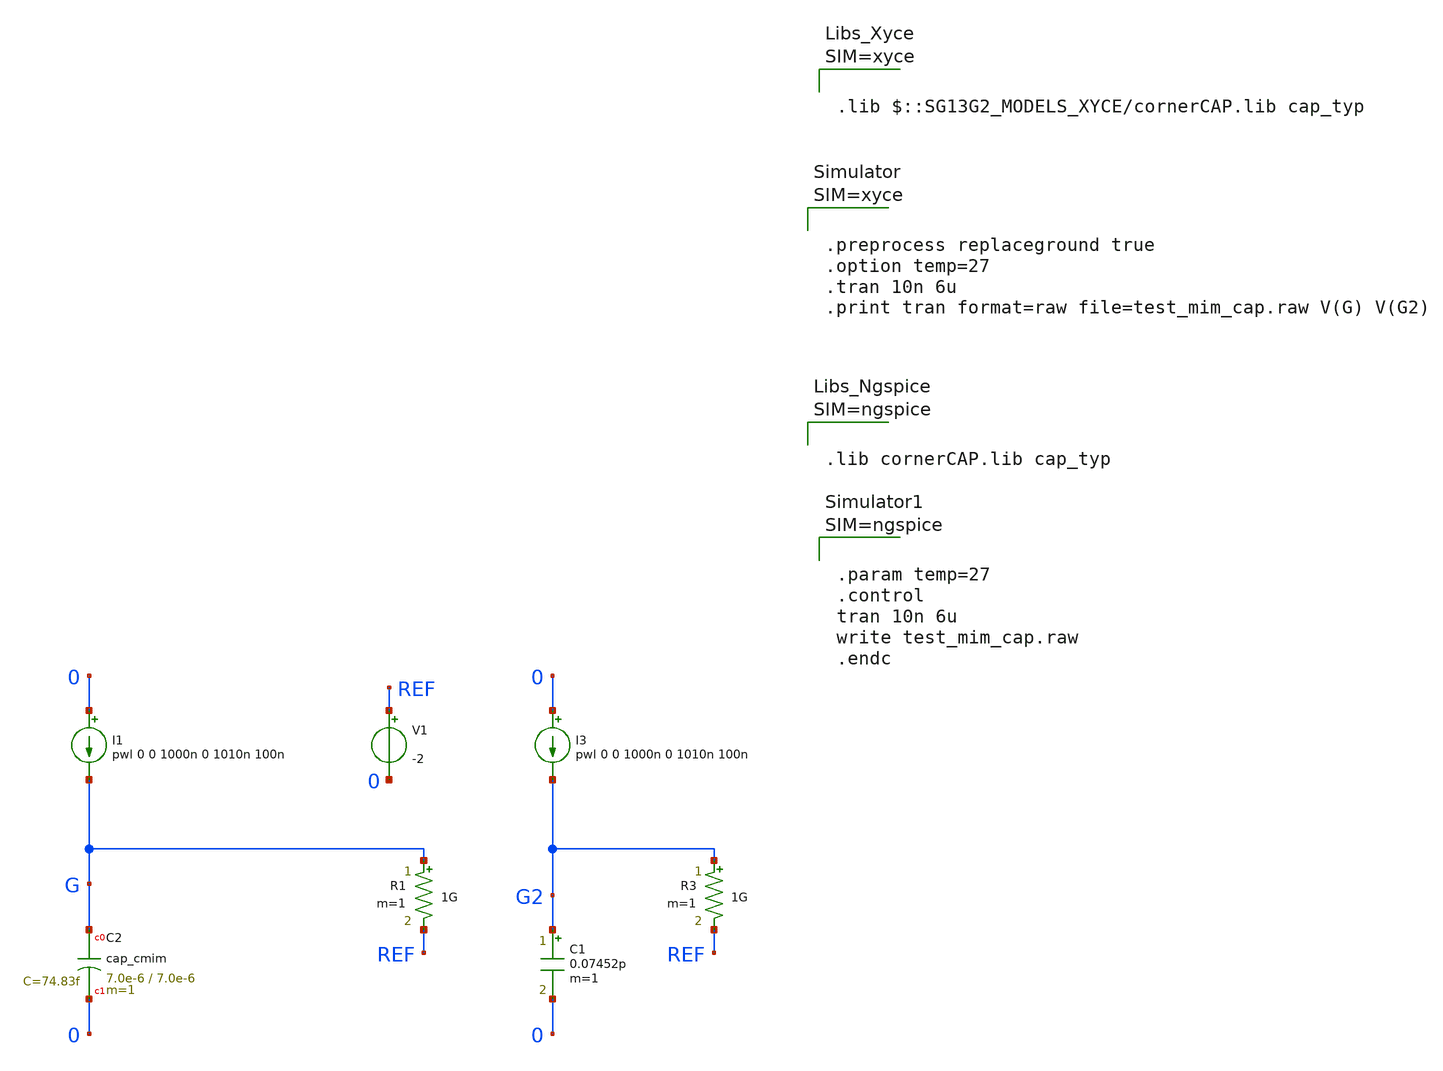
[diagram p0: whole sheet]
** sch_path: ihp-sg13g2/libs.tech/xschem/sg13g2_tests_xyce/tran_mim_cap.sch
* Copyright 2021 Stefan Frederik Schippers
* Licensed under the Apache License, Version 2.0 (the "License");
* you may not use this file except in compliance with the License.
* You may obtain a copy of the License at
* https://www.apache.org/licenses/LICENSE-2.0
* Unless required by applicable law or agreed to in writing, software
* distributed under the License is distributed on an "AS IS" BASIS,
* WITHOUT WARRANTIES OR CONDITIONS OF ANY KIND, either express or implied.
* See the License for the specific language governing permissions and
* limitations under the License.
* Copyright 2023 IHP PDK Authors
**.subckt tran_mim_cap
I1 0 G pwl 0 0 1000n 0 1010n 100n
R1 G REF 1G m=1
I3 0 G2 pwl 0 0 1000n 0 1010n 100n
R3 G2 REF 1G m=1
C1 G2 0 0.07452p m=1
V1 REF 0 -2
XC2 G 0 cap_cmim w=7.0e-6 l=7.0e-6 m=1 mm_ok=1
**** begin user architecture code









.lib cornerCAP.lib cap_typ






.param temp=27
.control
tran 10n 6u
write test_mim_cap.raw
.endc



**** end user architecture code
**.ends
.end
